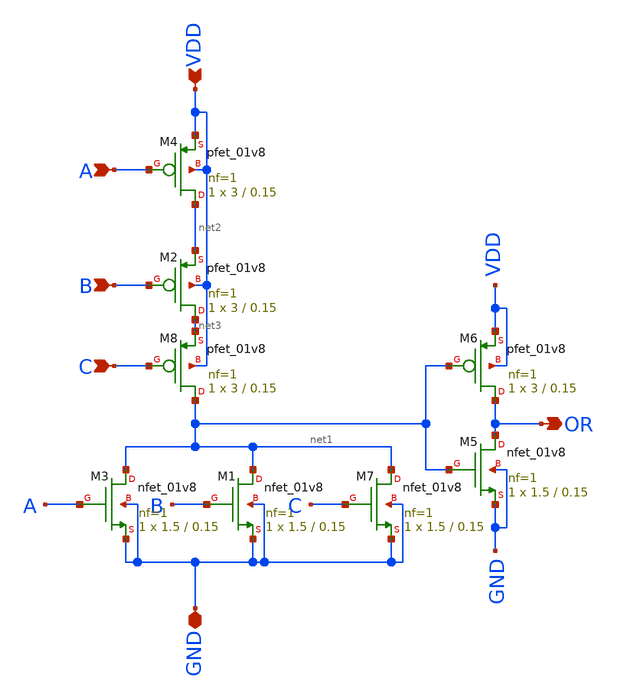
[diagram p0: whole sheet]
** sch_path: skywater_stuff/CMOS_3in_OR.sch
**.subckt CMOS_3in_OR A B C OR GND VDD
*.ipin A
*.ipin B
*.ipin C
*.opin OR
*.iopin GND
*.ipin VDD
XM4 net2 A VDD VDD sky130_fd_pr__pfet_01v8 L=0.15 W=3 nf=1 ad='int((nf+1)/2) * W/nf * 0.29' as='int((nf+2)/2) * W/nf * 0.29'
+ pd='2*int((nf+1)/2) * (W/nf + 0.29)' ps='2*int((nf+2)/2) * (W/nf + 0.29)' nrd='0.29 / W' nrs='0.29 / W'
+ sa=0 sb=0 sd=0 mult=1 m=1
XM2 net3 B net2 VDD sky130_fd_pr__pfet_01v8 L=0.15 W=3 nf=1 ad='int((nf+1)/2) * W/nf * 0.29' as='int((nf+2)/2) * W/nf * 0.29'
+ pd='2*int((nf+1)/2) * (W/nf + 0.29)' ps='2*int((nf+2)/2) * (W/nf + 0.29)' nrd='0.29 / W' nrs='0.29 / W'
+ sa=0 sb=0 sd=0 mult=1 m=1
XM5 OR net1 GND GND sky130_fd_pr__nfet_01v8 L=0.15 W=1.5 nf=1 ad='int((nf+1)/2) * W/nf * 0.29' as='int((nf+2)/2) * W/nf * 0.29'
+ pd='2*int((nf+1)/2) * (W/nf + 0.29)' ps='2*int((nf+2)/2) * (W/nf + 0.29)' nrd='0.29 / W' nrs='0.29 / W'
+ sa=0 sb=0 sd=0 mult=1 m=1
XM1 net1 B GND GND sky130_fd_pr__nfet_01v8 L=0.15 W=1.5 nf=1 ad='int((nf+1)/2) * W/nf * 0.29' as='int((nf+2)/2) * W/nf * 0.29'
+ pd='2*int((nf+1)/2) * (W/nf + 0.29)' ps='2*int((nf+2)/2) * (W/nf + 0.29)' nrd='0.29 / W' nrs='0.29 / W'
+ sa=0 sb=0 sd=0 mult=1 m=1
XM6 OR net1 VDD VDD sky130_fd_pr__pfet_01v8 L=0.15 W=3 nf=1 ad='int((nf+1)/2) * W/nf * 0.29' as='int((nf+2)/2) * W/nf * 0.29'
+ pd='2*int((nf+1)/2) * (W/nf + 0.29)' ps='2*int((nf+2)/2) * (W/nf + 0.29)' nrd='0.29 / W' nrs='0.29 / W'
+ sa=0 sb=0 sd=0 mult=1 m=1
XM7 net1 C GND GND sky130_fd_pr__nfet_01v8 L=0.15 W=1.5 nf=1 ad='int((nf+1)/2) * W/nf * 0.29' as='int((nf+2)/2) * W/nf * 0.29'
+ pd='2*int((nf+1)/2) * (W/nf + 0.29)' ps='2*int((nf+2)/2) * (W/nf + 0.29)' nrd='0.29 / W' nrs='0.29 / W'
+ sa=0 sb=0 sd=0 mult=1 m=1
XM3 net1 A GND GND sky130_fd_pr__nfet_01v8 L=0.15 W=1.5 nf=1 ad='int((nf+1)/2) * W/nf * 0.29' as='int((nf+2)/2) * W/nf * 0.29'
+ pd='2*int((nf+1)/2) * (W/nf + 0.29)' ps='2*int((nf+2)/2) * (W/nf + 0.29)' nrd='0.29 / W' nrs='0.29 / W'
+ sa=0 sb=0 sd=0 mult=1 m=1
XM8 net1 C net3 VDD sky130_fd_pr__pfet_01v8 L=0.15 W=3 nf=1 ad='int((nf+1)/2) * W/nf * 0.29' as='int((nf+2)/2) * W/nf * 0.29'
+ pd='2*int((nf+1)/2) * (W/nf + 0.29)' ps='2*int((nf+2)/2) * (W/nf + 0.29)' nrd='0.29 / W' nrs='0.29 / W'
+ sa=0 sb=0 sd=0 mult=1 m=1
**.ends
.end
